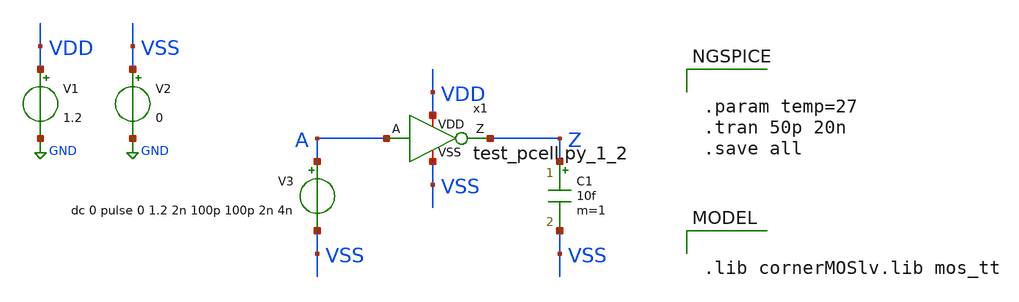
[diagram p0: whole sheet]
** sch_path: analog/tb/tb_inv_1x_gen.sch
**.subckt tb_inv_1x_gen
V1 VDD GND 1.2
C1 Z VSS 10f m=1
V2 VSS GND 0
V3 A VSS dc 0 pulse 0 1.2 2n 100p 100p 2n 4n
x1 VDD A Z VSS test_pcell.py_1_2
**** begin user architecture code


.param temp=27
.tran 50p 20n
.save all




.lib cornerMOSlv.lib mos_tt


**** end user architecture code
**.ends
.GLOBAL GND
.end
